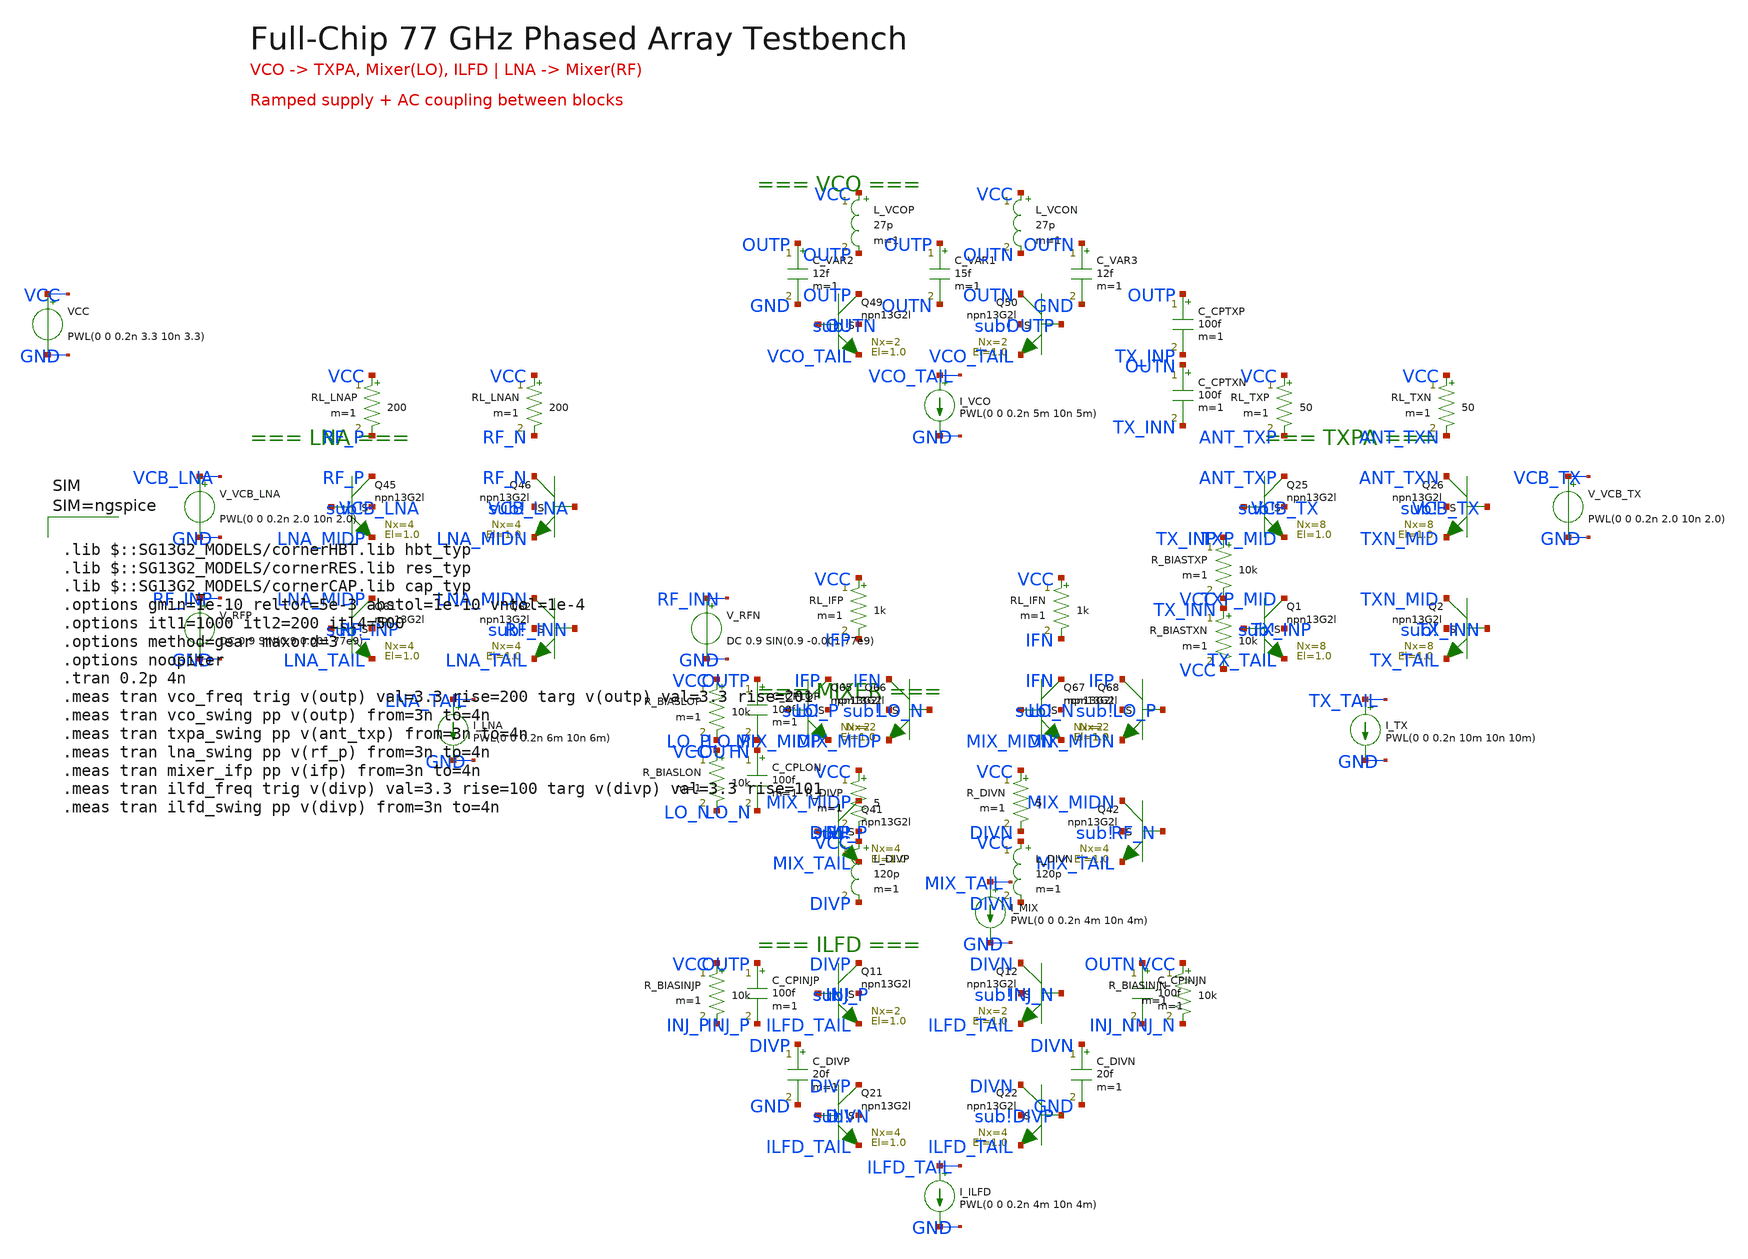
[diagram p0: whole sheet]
** sch_path: layout/testbenches/tb_fullchip.sch
**.subckt tb_fullchip
XQ49 OUTP OUTN VCO_TAIL sub! npn13G2l Nx=2 El=1.0 mm_ok=1
XQ50 OUTN OUTP VCO_TAIL sub! npn13G2l Nx=2 El=1.0 mm_ok=1
L_VCOP VCC OUTP 27p m=1
L_VCON VCC OUTN 27p m=1
C_VAR1 OUTP OUTN 15f m=1
C_VAR2 OUTP GND 12f m=1
C_VAR3 OUTN GND 12f m=1
I_VCO VCO_TAIL GND PWL(0 0 0.2n 5m 10n 5m)
XQ1 TXP_MID TX_INP TX_TAIL sub! npn13G2l Nx=8 El=1.0 mm_ok=1
XQ2 TXN_MID TX_INN TX_TAIL sub! npn13G2l Nx=8 El=1.0 mm_ok=1
XQ25 ANT_TXP VCB_TX TXP_MID sub! npn13G2l Nx=8 El=1.0 mm_ok=1
XQ26 ANT_TXN VCB_TX TXN_MID sub! npn13G2l Nx=8 El=1.0 mm_ok=1
RL_TXP VCC ANT_TXP 50 m=1
RL_TXN VCC ANT_TXN 50 m=1
C_CPTXP OUTP TX_INP 100f m=1
C_CPTXN OUTN TX_INN 100f m=1
R_BIASTXP TX_INP VCC 10k m=1
R_BIASTXN TX_INN VCC 10k m=1
I_TX TX_TAIL GND PWL(0 0 0.2n 10m 10n 10m)
V_VCB_TX VCB_TX GND PWL(0 0 0.2n 2.0 10n 2.0)
XQ61 LNA_MIDP RF_INP LNA_TAIL sub! npn13G2l Nx=4 El=1.0 mm_ok=1
XQ62 LNA_MIDN RF_INN LNA_TAIL sub! npn13G2l Nx=4 El=1.0 mm_ok=1
XQ45 RF_P VCB_LNA LNA_MIDP sub! npn13G2l Nx=4 El=1.0 mm_ok=1
XQ46 RF_N VCB_LNA LNA_MIDN sub! npn13G2l Nx=4 El=1.0 mm_ok=1
RL_LNAP VCC RF_P 200 m=1
RL_LNAN VCC RF_N 200 m=1
I_LNA LNA_TAIL GND PWL(0 0 0.2n 6m 10n 6m)
V_VCB_LNA VCB_LNA GND PWL(0 0 0.2n 2.0 10n 2.0)
V_RFP RF_INP GND DC 0.9 SIN(0.9 0.001 77e9)
V_RFN RF_INN GND DC 0.9 SIN(0.9 -0.001 77e9)
XQ41 MIX_MIDP RF_P MIX_TAIL sub! npn13G2l Nx=4 El=1.0 mm_ok=1
XQ42 MIX_MIDN RF_N MIX_TAIL sub! npn13G2l Nx=4 El=1.0 mm_ok=1
XQ65 IFP LO_P MIX_MIDP sub! npn13G2l Nx=2 El=1.0 mm_ok=1
XQ66 IFN LO_N MIX_MIDP sub! npn13G2l Nx=2 El=1.0 mm_ok=1
XQ67 IFN LO_N MIX_MIDN sub! npn13G2l Nx=2 El=1.0 mm_ok=1
XQ68 IFP LO_P MIX_MIDN sub! npn13G2l Nx=2 El=1.0 mm_ok=1
RL_IFP VCC IFP 1k m=1
RL_IFN VCC IFN 1k m=1
C_CPLOP OUTP LO_P 100f m=1
C_CPLON OUTN LO_N 100f m=1
R_BIASLOP VCC LO_P 10k m=1
R_BIASLON VCC LO_N 10k m=1
I_MIX MIX_TAIL GND PWL(0 0 0.2n 4m 10n 4m)
XQ21 DIVP DIVN ILFD_TAIL sub! npn13G2l Nx=4 El=1.0 mm_ok=1
XQ22 DIVN DIVP ILFD_TAIL sub! npn13G2l Nx=4 El=1.0 mm_ok=1
XQ11 DIVP INJ_P ILFD_TAIL sub! npn13G2l Nx=2 El=1.0 mm_ok=1
XQ12 DIVN INJ_N ILFD_TAIL sub! npn13G2l Nx=2 El=1.0 mm_ok=1
L_DIVP VCC DIVP 120p m=1
L_DIVN VCC DIVN 120p m=1
R_DIVP VCC sub! 5 m=1
R_DIVN VCC DIVN 5 m=1
C_DIVP DIVP GND 20f m=1
C_DIVN DIVN GND 20f m=1
C_CPINJP OUTP INJ_P 100f m=1
C_CPINJN OUTN INJ_N 100f m=1
R_BIASINJP VCC INJ_P 10k m=1
R_BIASINJN VCC INJ_N 10k m=1
I_ILFD ILFD_TAIL GND PWL(0 0 0.2n 4m 10n 4m)
VCC VCC GND PWL(0 0 0.2n 3.3 10n 3.3)
**** begin user architecture code



.lib $::SG13G2_MODELS/cornerHBT.lib hbt_typ
.lib $::SG13G2_MODELS/cornerRES.lib res_typ
.lib $::SG13G2_MODELS/cornerCAP.lib cap_typ
.options gmin=1e-10 reltol=5e-3 abstol=1e-10 vntol=1e-4
.options itl1=1000 itl2=200 itl4=500
.options method=gear maxord=3
.options noopiter
.tran 0.2p 4n
.meas tran vco_freq trig v(outp) val=3.3 rise=200 targ v(outp) val=3.3 rise=201
.meas tran vco_swing pp v(outp) from=3n to=4n
.meas tran txpa_swing pp v(ant_txp) from=3n to=4n
.meas tran lna_swing pp v(rf_p) from=3n to=4n
.meas tran mixer_ifp pp v(ifp) from=3n to=4n
.meas tran ilfd_freq trig v(divp) val=3.3 rise=100 targ v(divp) val=3.3 rise=101
.meas tran ilfd_swing pp v(divp) from=3n to=4n



**** end user architecture code
**.ends
.end
